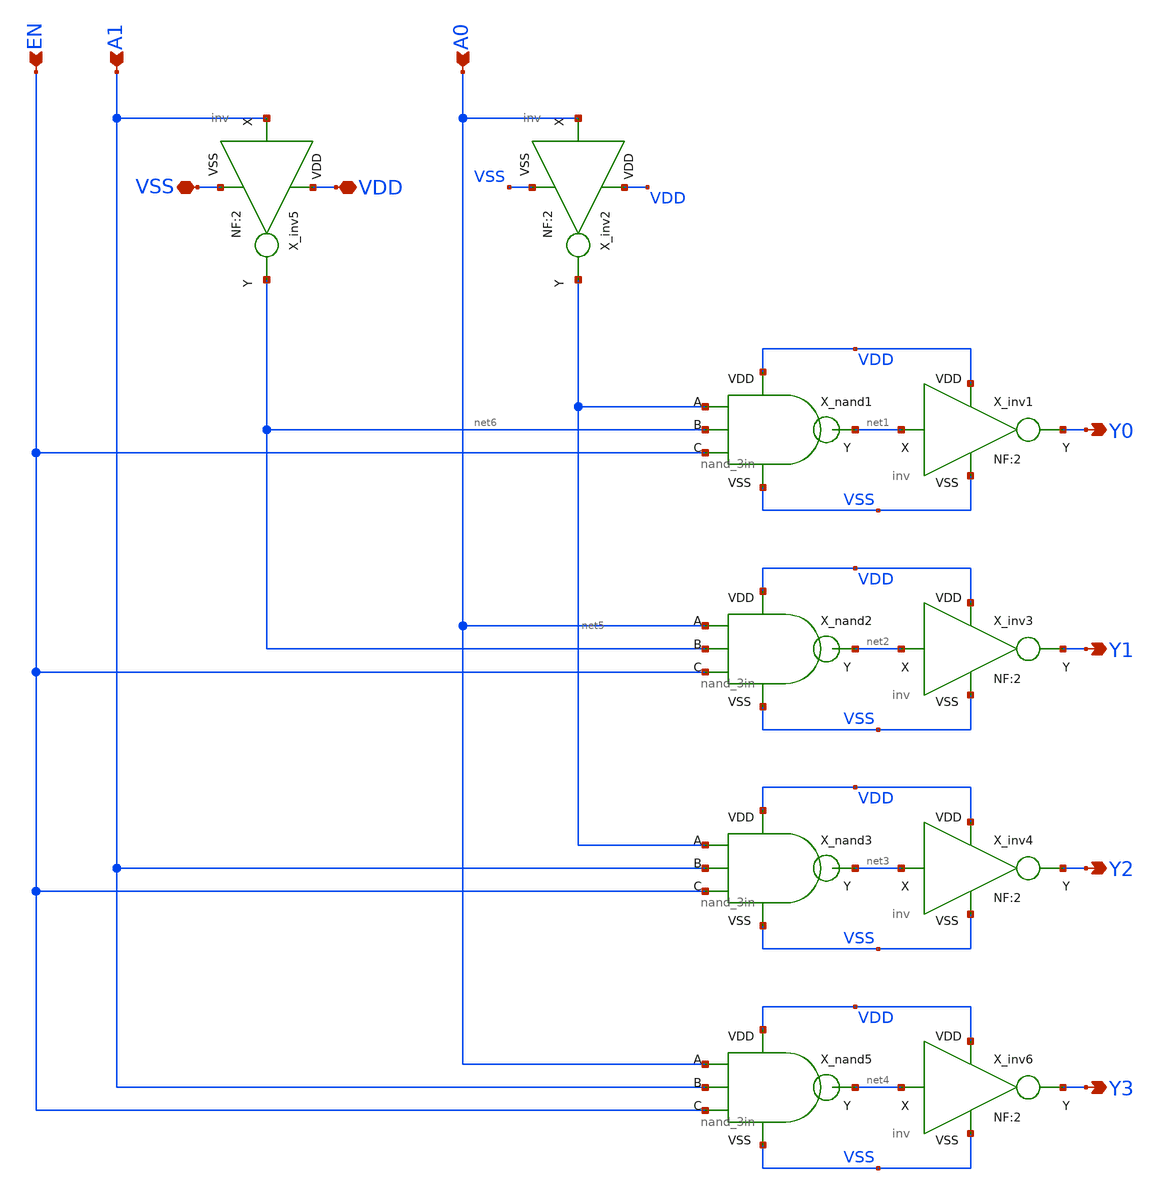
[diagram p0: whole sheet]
** sch_path: xschem_lib/DFFRAM_full_custom/dec_2to4.sch
**.subckt dec_2to4 A0 A1 VDD VSS EN Y0 Y1 Y2 Y3
*.ipin A0
*.ipin A1
*.iopin VDD
*.iopin VSS
*.ipin EN
*.opin Y0
*.opin Y1
*.opin Y2
*.opin Y3
X_nand1 net5 net6 EN net1 VDD VSS nand_3in
X_inv1 net1 VDD VSS Y0 inv NF=2
X_nand2 A0 net6 EN net2 VDD VSS nand_3in
X_inv3 net2 VDD VSS Y1 inv NF=2
X_nand3 net5 A1 EN net3 VDD VSS nand_3in
X_inv4 net3 VDD VSS Y2 inv NF=2
X_nand5 A0 A1 EN net4 VDD VSS nand_3in
X_inv6 net4 VDD VSS Y3 inv NF=2
X_inv2 A0 VDD VSS net5 inv NF=2
X_inv5 A1 VDD VSS net6 inv NF=2
**.ends

* expanding   symbol:  xschem_lib/DFFRAM_full_custom/nand_3in.sym # of pins=6
** sym_path: xschem_lib/DFFRAM_full_custom/nand_3in.sym
** sch_path: xschem_lib/DFFRAM_full_custom/nand_3in.sch
.subckt nand_3in A B C Y VDD VSS
*.iopin VDD
*.opin Y
*.iopin VSS
*.ipin A
*.ipin B
*.ipin C
XM1 Y A net1 VSS sky130_fd_pr__nfet_01v8_lvt L=0.15 W=2*1.2 nf=2 ad='int((nf+1)/2) * W/nf * 0.29' as='int((nf+2)/2) * W/nf * 0.29'
+ pd='2*int((nf+1)/2) * (W/nf + 0.29)' ps='2*int((nf+2)/2) * (W/nf + 0.29)' nrd='0.29 / W' nrs='0.29 / W'
+ sa=0 sb=0 sd=0 mult=1 m=1
XM5 Y A VDD VDD sky130_fd_pr__pfet_01v8 L=0.15 W=2*2.4 nf=2 ad='int((nf+1)/2) * W/nf * 0.29' as='int((nf+2)/2) * W/nf * 0.29'
+ pd='2*int((nf+1)/2) * (W/nf + 0.29)' ps='2*int((nf+2)/2) * (W/nf + 0.29)' nrd='0.29 / W' nrs='0.29 / W'
+ sa=0 sb=0 sd=0 mult=1 m=1
XM4 Y B VDD VDD sky130_fd_pr__pfet_01v8 L=0.15 W=2*2.4 nf=2 ad='int((nf+1)/2) * W/nf * 0.29' as='int((nf+2)/2) * W/nf * 0.29'
+ pd='2*int((nf+1)/2) * (W/nf + 0.29)' ps='2*int((nf+2)/2) * (W/nf + 0.29)' nrd='0.29 / W' nrs='0.29 / W'
+ sa=0 sb=0 sd=0 mult=1 m=1
XM6 Y C VDD VDD sky130_fd_pr__pfet_01v8 L=0.15 W=2*2.4 nf=2 ad='int((nf+1)/2) * W/nf * 0.29' as='int((nf+2)/2) * W/nf * 0.29'
+ pd='2*int((nf+1)/2) * (W/nf + 0.29)' ps='2*int((nf+2)/2) * (W/nf + 0.29)' nrd='0.29 / W' nrs='0.29 / W'
+ sa=0 sb=0 sd=0 mult=1 m=1
XM2 net1 B net2 VSS sky130_fd_pr__nfet_01v8_lvt L=0.15 W=2*1.2 nf=2 ad='int((nf+1)/2) * W/nf * 0.29'
+ as='int((nf+2)/2) * W/nf * 0.29' pd='2*int((nf+1)/2) * (W/nf + 0.29)' ps='2*int((nf+2)/2) * (W/nf + 0.29)'
+ nrd='0.29 / W' nrs='0.29 / W' sa=0 sb=0 sd=0 mult=1 m=1
XM3 net2 C VSS VSS sky130_fd_pr__nfet_01v8_lvt L=0.15 W=2*1.2 nf=2 ad='int((nf+1)/2) * W/nf * 0.29' as='int((nf+2)/2) * W/nf * 0.29'
+ pd='2*int((nf+1)/2) * (W/nf + 0.29)' ps='2*int((nf+2)/2) * (W/nf + 0.29)' nrd='0.29 / W' nrs='0.29 / W'
+ sa=0 sb=0 sd=0 mult=1 m=1
.ends


* expanding   symbol:  xschem_lib/DFFRAM_full_custom/inv.sym # of pins=4
** sym_path: xschem_lib/DFFRAM_full_custom/inv.sym
** sch_path: xschem_lib/DFFRAM_full_custom/inv.sch
.subckt inv X VDD VSS Y  NF=2
*.iopin VSS
*.ipin X
*.opin Y
*.iopin VDD
XM1 Y X VSS VSS sky130_fd_pr__nfet_01v8_lvt L=0.15 W=NF*0.5 nf=NF ad='int((nf+1)/2) * W/nf * 0.29' as='int((nf+2)/2) * W/nf * 0.29'
+ pd='2*int((nf+1)/2) * (W/nf + 0.29)' ps='2*int((nf+2)/2) * (W/nf + 0.29)' nrd='0.29 / W' nrs='0.29 / W'
+ sa=0 sb=0 sd=0 mult=1 m=1
XM2 Y X VDD VDD sky130_fd_pr__pfet_01v8 L=0.15 W=NF*1 nf=NF ad='int((nf+1)/2) * W/nf * 0.29' as='int((nf+2)/2) * W/nf * 0.29'
+ pd='2*int((nf+1)/2) * (W/nf + 0.29)' ps='2*int((nf+2)/2) * (W/nf + 0.29)' nrd='0.29 / W' nrs='0.29 / W'
+ sa=0 sb=0 sd=0 mult=1 m=1
.ends

.end
